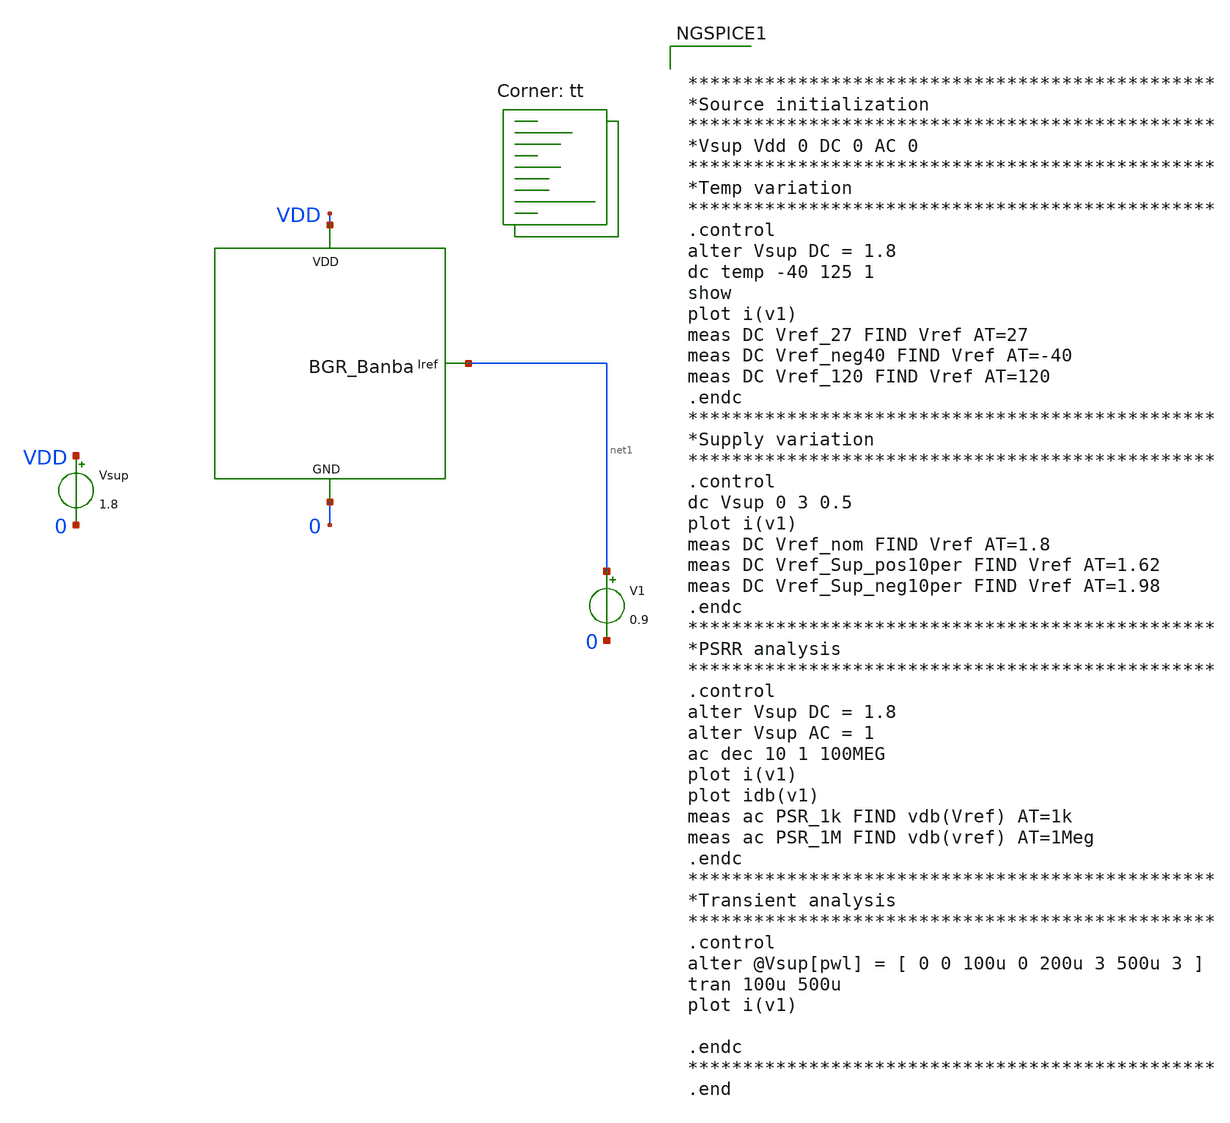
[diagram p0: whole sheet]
** sch_path: pll/lc_vco_lib_Hossam_Tarek/BGR_Banba_tb/xschem/BGR_Banba_tb.sch
**.subckt BGR_Banba_tb
Vsup VDD 0 1.8
V1 net1 0 0.9
X1 net1 0 VDD BGR_Banba
**** begin user architecture code


************************************************
*Source initialization
************************************************
*Vsup Vdd 0 DC 0 AC 0
************************************************
*Temp variation
************************************************
.control
alter Vsup DC = 1.8
dc temp -40 125 1
show
plot i(v1)
meas DC Vref_27 FIND Vref AT=27
meas DC Vref_neg40 FIND Vref AT=-40
meas DC Vref_120 FIND Vref AT=120
.endc
************************************************
*Supply variation
************************************************
.control
dc Vsup 0 3 0.5
plot i(v1)
meas DC Vref_nom FIND Vref AT=1.8
meas DC Vref_Sup_pos10per FIND Vref AT=1.62
meas DC Vref_Sup_neg10per FIND Vref AT=1.98
.endc
************************************************
*PSRR analysis
************************************************
.control
alter Vsup DC = 1.8
alter Vsup AC = 1
ac dec 10 1 100MEG
plot i(v1)
plot idb(v1)
meas ac PSR_1k FIND vdb(Vref) AT=1k
meas ac PSR_1M FIND vdb(vref) AT=1Meg
.endc
************************************************
*Transient analysis
************************************************
.control
alter @Vsup[pwl] = [ 0 0 100u 0 200u 3 500u 3 ]
tran 100u 500u
plot i(v1)

.endc
************************************************
.end


.lib $::SKYWATER_MODELS/sky130.lib.spice tt
**** end user architecture code
**.ends
.end
